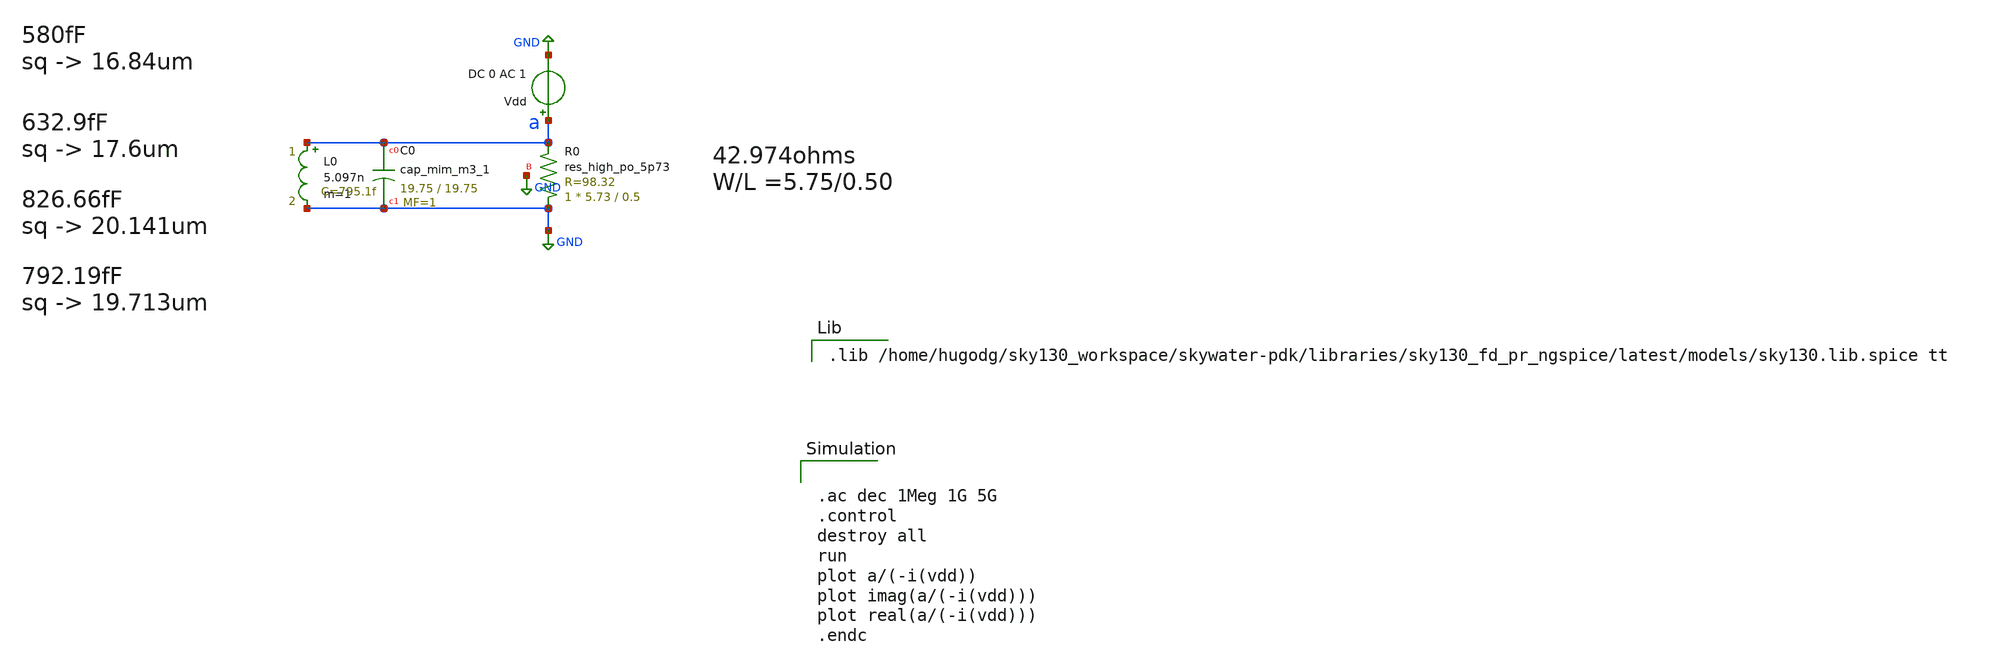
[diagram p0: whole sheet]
** sch_path: ask_modulator/xschem/rlc_tb-ac.sch
**.subckt rlc_tb-ac
L0 a GND 5.097n m=1
Vdd a GND DC 0 AC 1
XR0 GND a GND sky130_fd_pr__res_high_po_5p73 L=0.5 mult=1 m=1
XC0 a GND sky130_fd_pr__cap_mim_m3_1 W=19.75 L=19.75 MF=1 m=1
**** begin user architecture code

.lib /home/hugodg/sky130_workspace/skywater-pdk/libraries/sky130_fd_pr_ngspice/latest/models/sky130.lib.spice tt



.ac dec 1Meg 1G 5G
.control
destroy all
run
plot a/(-i(vdd))
plot imag(a/(-i(vdd)))
plot real(a/(-i(vdd)))
.endc

**** end user architecture code
**.ends
.GLOBAL GND
.end
